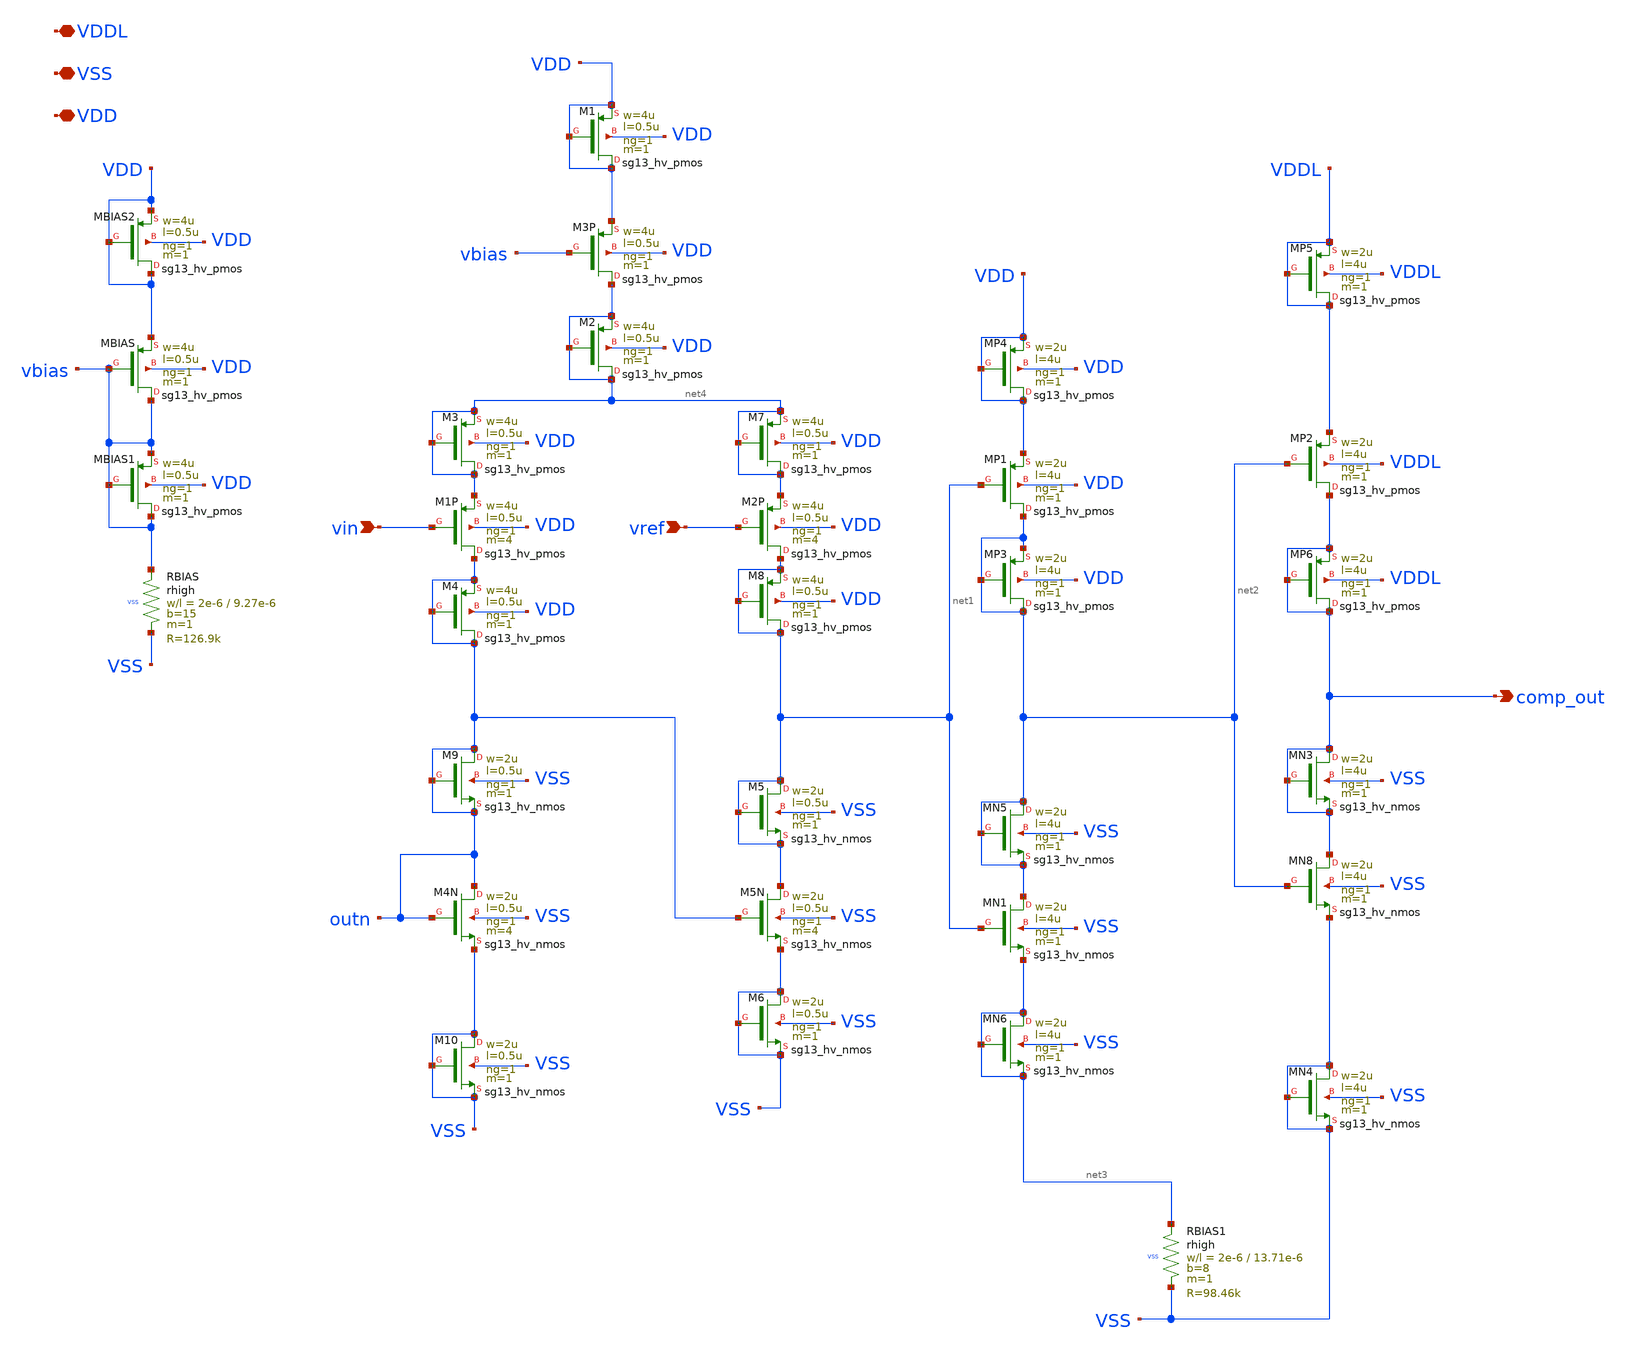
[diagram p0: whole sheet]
** sch_path: macros/heichips26_ook/macros/ook_analog_system/schematic/xschem/simple_comparator.sch
**.subckt simple_comparator vin vref VDD VSS comp_out VDDL
*.ipin vin
*.ipin vref
*.iopin VDD
*.iopin VSS
*.opin comp_out
*.iopin VDDL
XMBIAS vbias vbias VDD VDD sg13_hv_pmos w=4u l=0.5u ng=1 m=1 mm_ok=1
XRBIAS vbias VSS VSS rhigh w=2e-6 l=9.27e-6 m=1 b=15 ps=0.18e-6 mm_ok=1
XM3P net4 vbias VDD VDD sg13_hv_pmos w=4u l=0.5u ng=1 m=1 mm_ok=1
XM1P outn vin net4 VDD sg13_hv_pmos w=4u l=0.5u ng=1 m=4 mm_ok=1
XM2P net1 vref net4 VDD sg13_hv_pmos w=4u l=0.5u ng=1 m=4 mm_ok=1
XM4N outn outn VSS VSS sg13_hv_nmos w=2u l=0.5u ng=1 m=4 mm_ok=1
XM5N net1 outn VSS VSS sg13_hv_nmos w=2u l=0.5u ng=1 m=4 mm_ok=1
XMP1 net2 net1 VDD VDD sg13_hv_pmos w=2u l=4u ng=1 m=1 mm_ok=1
XMN1 net2 net1 net3 VSS sg13_hv_nmos w=2u l=4u ng=1 m=1 mm_ok=1
XMP2 comp_out net2 VDDL VDDL sg13_hv_pmos w=2u l=4u ng=1 m=1 mm_ok=1
XMBIAS1 vbias vbias vbias VDD sg13_hv_pmos w=4u l=0.5u ng=1 m=1 mm_ok=1
XMBIAS2 VDD VDD VDD VDD sg13_hv_pmos w=4u l=0.5u ng=1 m=1 mm_ok=1
XM1 VDD VDD VDD VDD sg13_hv_pmos w=4u l=0.5u ng=1 m=1 mm_ok=1
XM2 net4 net4 net4 VDD sg13_hv_pmos w=4u l=0.5u ng=1 m=1 mm_ok=1
XMP3 net2 net2 net2 VDD sg13_hv_pmos w=2u l=4u ng=1 m=1 mm_ok=1
XMP4 VDD VDD VDD VDD sg13_hv_pmos w=2u l=4u ng=1 m=1 mm_ok=1
XMP5 VDDL VDDL VDDL VDDL sg13_hv_pmos w=2u l=4u ng=1 m=1 mm_ok=1
XMP6 comp_out comp_out comp_out VDDL sg13_hv_pmos w=2u l=4u ng=1 m=1 mm_ok=1
XMN3 comp_out comp_out comp_out VSS sg13_hv_nmos w=2u l=4u ng=1 m=1 mm_ok=1
XMN4 VSS VSS VSS VSS sg13_hv_nmos w=2u l=4u ng=1 m=1 mm_ok=1
XMN5 net2 net2 net2 VSS sg13_hv_nmos w=2u l=4u ng=1 m=1 mm_ok=1
XMN6 net3 net3 net3 VSS sg13_hv_nmos w=2u l=4u ng=1 m=1 mm_ok=1
XM3 net4 net4 net4 VDD sg13_hv_pmos w=4u l=0.5u ng=1 m=1 mm_ok=1
XM4 outn outn outn VDD sg13_hv_pmos w=4u l=0.5u ng=1 m=1 mm_ok=1
XM5 net1 net1 net1 VSS sg13_hv_nmos w=2u l=0.5u ng=1 m=1 mm_ok=1
XM6 VSS VSS VSS VSS sg13_hv_nmos w=2u l=0.5u ng=1 m=1 mm_ok=1
XM7 net4 net4 net4 VDD sg13_hv_pmos w=4u l=0.5u ng=1 m=1 mm_ok=1
XM8 net1 net1 net1 VDD sg13_hv_pmos w=4u l=0.5u ng=1 m=1 mm_ok=1
XM9 outn outn outn VSS sg13_hv_nmos w=2u l=0.5u ng=1 m=1 mm_ok=1
XM10 VSS VSS VSS VSS sg13_hv_nmos w=2u l=0.5u ng=1 m=1 mm_ok=1
XRBIAS1 net3 VSS VSS rhigh w=2e-6 l=13.71e-6 m=1 b=8 ps=0.18e-6 mm_ok=1
XMN8 comp_out net2 VSS VSS sg13_hv_nmos w=2u l=4u ng=1 m=1 mm_ok=1
**.ends
.end
